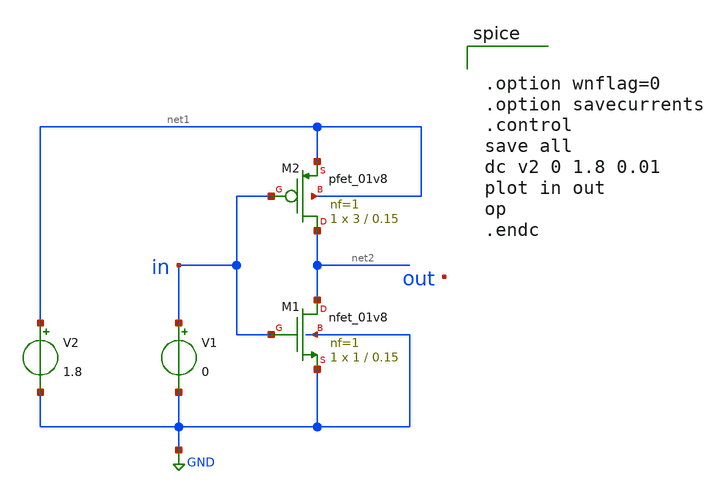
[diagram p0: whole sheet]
** sch_path: untitled.sch
**.subckt untitled
XM1 net2 in GND GND sky130_fd_pr__nfet_01v8 L=0.15 W=1 nf=1 ad='int((nf+1)/2) * W/nf * 0.29' as='int((nf+2)/2) * W/nf * 0.29'
+ pd='2*int((nf+1)/2) * (W/nf + 0.29)' ps='2*int((nf+2)/2) * (W/nf + 0.29)' nrd='0.29 / W' nrs='0.29 / W'
+ sa=0 sb=0 sd=0 mult=1 m=1
V1 in GND 0
V2 net1 GND 1.8
XM2 net2 in net1 net1 sky130_fd_pr__pfet_01v8 L=0.15 W=3 nf=1 ad='int((nf+1)/2) * W/nf * 0.29' as='int((nf+2)/2) * W/nf * 0.29'
+ pd='2*int((nf+1)/2) * (W/nf + 0.29)' ps='2*int((nf+2)/2) * (W/nf + 0.29)' nrd='0.29 / W' nrs='0.29 / W'
+ sa=0 sb=0 sd=0 mult=1 m=1
**** begin user architecture code



.option wnflag=0
.option savecurrents
.control
save all
dc v2 0 1.8 0.01
plot in out
op
.endc


**** end user architecture code
**.ends
.GLOBAL GND
.end
